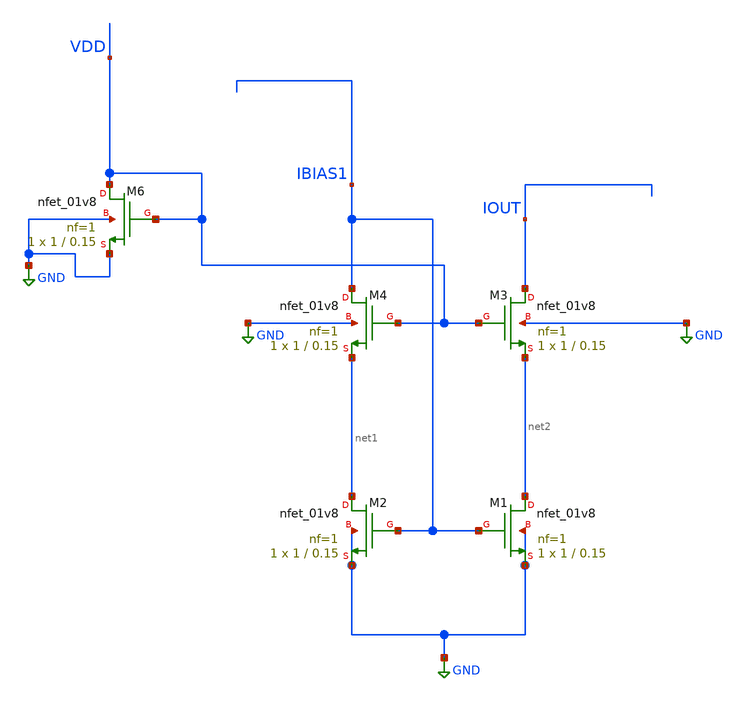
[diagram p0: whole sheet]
** sch_path: xschem/DC_DC_Converter_xschem/OTHERS/DC_DC_Converter_5/LV_Current_mirror.sch
**.subckt LV_Current_mirror
XM1 net2 IBIAS1 GND GND sky130_fd_pr__nfet_01v8 L=0.15 W=1 nf=1 ad='int((nf+1)/2) * W/nf * 0.29' as='int((nf+2)/2) * W/nf * 0.29'
+ pd='2*int((nf+1)/2) * (W/nf + 0.29)' ps='2*int((nf+2)/2) * (W/nf + 0.29)' nrd='0.29 / W' nrs='0.29 / W'
+ sa=0 sb=0 sd=0 mult=1 m=1
XM2 net1 IBIAS1 GND GND sky130_fd_pr__nfet_01v8 L=0.15 W=1 nf=1 ad='int((nf+1)/2) * W/nf * 0.29' as='int((nf+2)/2) * W/nf * 0.29'
+ pd='2*int((nf+1)/2) * (W/nf + 0.29)' ps='2*int((nf+2)/2) * (W/nf + 0.29)' nrd='0.29 / W' nrs='0.29 / W'
+ sa=0 sb=0 sd=0 mult=1 m=1
XM3 IOUT VDD net2 GND sky130_fd_pr__nfet_01v8 L=0.15 W=1 nf=1 ad='int((nf+1)/2) * W/nf * 0.29' as='int((nf+2)/2) * W/nf * 0.29'
+ pd='2*int((nf+1)/2) * (W/nf + 0.29)' ps='2*int((nf+2)/2) * (W/nf + 0.29)' nrd='0.29 / W' nrs='0.29 / W'
+ sa=0 sb=0 sd=0 mult=1 m=1
XM4 IBIAS1 VDD net1 GND sky130_fd_pr__nfet_01v8 L=0.15 W=1 nf=1 ad='int((nf+1)/2) * W/nf * 0.29' as='int((nf+2)/2) * W/nf * 0.29'
+ pd='2*int((nf+1)/2) * (W/nf + 0.29)' ps='2*int((nf+2)/2) * (W/nf + 0.29)' nrd='0.29 / W' nrs='0.29 / W'
+ sa=0 sb=0 sd=0 mult=1 m=1
XM6 VDD VDD GND GND sky130_fd_pr__nfet_01v8 L=0.15 W=1 nf=1 ad='int((nf+1)/2) * W/nf * 0.29' as='int((nf+2)/2) * W/nf * 0.29'
+ pd='2*int((nf+1)/2) * (W/nf + 0.29)' ps='2*int((nf+2)/2) * (W/nf + 0.29)' nrd='0.29 / W' nrs='0.29 / W'
+ sa=0 sb=0 sd=0 mult=1 m=1
**.ends
.GLOBAL GND
.end
